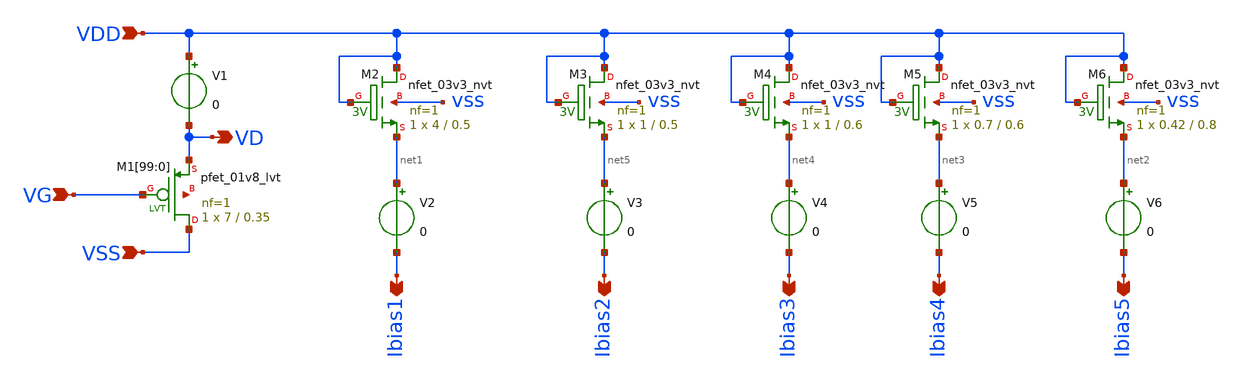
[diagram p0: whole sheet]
** sch_path: design/THESIS_EXP_RO_INVERTER_SKY130A/TB_FET.sch
**.subckt TB_FET VDD VSS VD VG Ibias1 Ibias2 Ibias3 Ibias4 Ibias5
*.ipin VDD
*.ipin VSS
*.opin VD
*.ipin VG
*.opin Ibias1
*.opin Ibias2
*.opin Ibias3
*.opin Ibias4
*.opin Ibias5
V1 VDD VD 0
.save i(v1)
XM1[99] VSS VG VD net6[99] sky130_fd_pr__pfet_01v8_lvt L=0.35 W=7 nf=1 ad='int((1 + 1)/2) * 7 / 1 * 0.29'
+ as='int((1 + 2)/2) * 7 / 1 * 0.29' pd='2*int((1 + 1)/2) * (7 / 1 + 0.29)' ps='2*int((1 + 2)/2) * (7 / 1 + 0.29)'
+ nrd='0.29 / 7 ' nrs='0.29 / 7 ' sa=0 sb=0 sd=0 mult=1 m=1
XM1[98] VSS VG VD net6[98] sky130_fd_pr__pfet_01v8_lvt L=0.35 W=7 nf=1 ad='int((1 + 1)/2) * 7 / 1 * 0.29'
+ as='int((1 + 2)/2) * 7 / 1 * 0.29' pd='2*int((1 + 1)/2) * (7 / 1 + 0.29)' ps='2*int((1 + 2)/2) * (7 / 1 + 0.29)'
+ nrd='0.29 / 7 ' nrs='0.29 / 7 ' sa=0 sb=0 sd=0 mult=1 m=1
XM1[97] VSS VG VD net6[97] sky130_fd_pr__pfet_01v8_lvt L=0.35 W=7 nf=1 ad='int((1 + 1)/2) * 7 / 1 * 0.29'
+ as='int((1 + 2)/2) * 7 / 1 * 0.29' pd='2*int((1 + 1)/2) * (7 / 1 + 0.29)' ps='2*int((1 + 2)/2) * (7 / 1 + 0.29)'
+ nrd='0.29 / 7 ' nrs='0.29 / 7 ' sa=0 sb=0 sd=0 mult=1 m=1
XM1[96] VSS VG VD net6[96] sky130_fd_pr__pfet_01v8_lvt L=0.35 W=7 nf=1 ad='int((1 + 1)/2) * 7 / 1 * 0.29'
+ as='int((1 + 2)/2) * 7 / 1 * 0.29' pd='2*int((1 + 1)/2) * (7 / 1 + 0.29)' ps='2*int((1 + 2)/2) * (7 / 1 + 0.29)'
+ nrd='0.29 / 7 ' nrs='0.29 / 7 ' sa=0 sb=0 sd=0 mult=1 m=1
XM1[95] VSS VG VD net6[95] sky130_fd_pr__pfet_01v8_lvt L=0.35 W=7 nf=1 ad='int((1 + 1)/2) * 7 / 1 * 0.29'
+ as='int((1 + 2)/2) * 7 / 1 * 0.29' pd='2*int((1 + 1)/2) * (7 / 1 + 0.29)' ps='2*int((1 + 2)/2) * (7 / 1 + 0.29)'
+ nrd='0.29 / 7 ' nrs='0.29 / 7 ' sa=0 sb=0 sd=0 mult=1 m=1
XM1[94] VSS VG VD net6[94] sky130_fd_pr__pfet_01v8_lvt L=0.35 W=7 nf=1 ad='int((1 + 1)/2) * 7 / 1 * 0.29'
+ as='int((1 + 2)/2) * 7 / 1 * 0.29' pd='2*int((1 + 1)/2) * (7 / 1 + 0.29)' ps='2*int((1 + 2)/2) * (7 / 1 + 0.29)'
+ nrd='0.29 / 7 ' nrs='0.29 / 7 ' sa=0 sb=0 sd=0 mult=1 m=1
XM1[93] VSS VG VD net6[93] sky130_fd_pr__pfet_01v8_lvt L=0.35 W=7 nf=1 ad='int((1 + 1)/2) * 7 / 1 * 0.29'
+ as='int((1 + 2)/2) * 7 / 1 * 0.29' pd='2*int((1 + 1)/2) * (7 / 1 + 0.29)' ps='2*int((1 + 2)/2) * (7 / 1 + 0.29)'
+ nrd='0.29 / 7 ' nrs='0.29 / 7 ' sa=0 sb=0 sd=0 mult=1 m=1
XM1[92] VSS VG VD net6[92] sky130_fd_pr__pfet_01v8_lvt L=0.35 W=7 nf=1 ad='int((1 + 1)/2) * 7 / 1 * 0.29'
+ as='int((1 + 2)/2) * 7 / 1 * 0.29' pd='2*int((1 + 1)/2) * (7 / 1 + 0.29)' ps='2*int((1 + 2)/2) * (7 / 1 + 0.29)'
+ nrd='0.29 / 7 ' nrs='0.29 / 7 ' sa=0 sb=0 sd=0 mult=1 m=1
XM1[91] VSS VG VD net6[91] sky130_fd_pr__pfet_01v8_lvt L=0.35 W=7 nf=1 ad='int((1 + 1)/2) * 7 / 1 * 0.29'
+ as='int((1 + 2)/2) * 7 / 1 * 0.29' pd='2*int((1 + 1)/2) * (7 / 1 + 0.29)' ps='2*int((1 + 2)/2) * (7 / 1 + 0.29)'
+ nrd='0.29 / 7 ' nrs='0.29 / 7 ' sa=0 sb=0 sd=0 mult=1 m=1
XM1[90] VSS VG VD net6[90] sky130_fd_pr__pfet_01v8_lvt L=0.35 W=7 nf=1 ad='int((1 + 1)/2) * 7 / 1 * 0.29'
+ as='int((1 + 2)/2) * 7 / 1 * 0.29' pd='2*int((1 + 1)/2) * (7 / 1 + 0.29)' ps='2*int((1 + 2)/2) * (7 / 1 + 0.29)'
+ nrd='0.29 / 7 ' nrs='0.29 / 7 ' sa=0 sb=0 sd=0 mult=1 m=1
XM1[89] VSS VG VD net6[89] sky130_fd_pr__pfet_01v8_lvt L=0.35 W=7 nf=1 ad='int((1 + 1)/2) * 7 / 1 * 0.29'
+ as='int((1 + 2)/2) * 7 / 1 * 0.29' pd='2*int((1 + 1)/2) * (7 / 1 + 0.29)' ps='2*int((1 + 2)/2) * (7 / 1 + 0.29)'
+ nrd='0.29 / 7 ' nrs='0.29 / 7 ' sa=0 sb=0 sd=0 mult=1 m=1
XM1[88] VSS VG VD net6[88] sky130_fd_pr__pfet_01v8_lvt L=0.35 W=7 nf=1 ad='int((1 + 1)/2) * 7 / 1 * 0.29'
+ as='int((1 + 2)/2) * 7 / 1 * 0.29' pd='2*int((1 + 1)/2) * (7 / 1 + 0.29)' ps='2*int((1 + 2)/2) * (7 / 1 + 0.29)'
+ nrd='0.29 / 7 ' nrs='0.29 / 7 ' sa=0 sb=0 sd=0 mult=1 m=1
XM1[87] VSS VG VD net6[87] sky130_fd_pr__pfet_01v8_lvt L=0.35 W=7 nf=1 ad='int((1 + 1)/2) * 7 / 1 * 0.29'
+ as='int((1 + 2)/2) * 7 / 1 * 0.29' pd='2*int((1 + 1)/2) * (7 / 1 + 0.29)' ps='2*int((1 + 2)/2) * (7 / 1 + 0.29)'
+ nrd='0.29 / 7 ' nrs='0.29 / 7 ' sa=0 sb=0 sd=0 mult=1 m=1
XM1[86] VSS VG VD net6[86] sky130_fd_pr__pfet_01v8_lvt L=0.35 W=7 nf=1 ad='int((1 + 1)/2) * 7 / 1 * 0.29'
+ as='int((1 + 2)/2) * 7 / 1 * 0.29' pd='2*int((1 + 1)/2) * (7 / 1 + 0.29)' ps='2*int((1 + 2)/2) * (7 / 1 + 0.29)'
+ nrd='0.29 / 7 ' nrs='0.29 / 7 ' sa=0 sb=0 sd=0 mult=1 m=1
XM1[85] VSS VG VD net6[85] sky130_fd_pr__pfet_01v8_lvt L=0.35 W=7 nf=1 ad='int((1 + 1)/2) * 7 / 1 * 0.29'
+ as='int((1 + 2)/2) * 7 / 1 * 0.29' pd='2*int((1 + 1)/2) * (7 / 1 + 0.29)' ps='2*int((1 + 2)/2) * (7 / 1 + 0.29)'
+ nrd='0.29 / 7 ' nrs='0.29 / 7 ' sa=0 sb=0 sd=0 mult=1 m=1
XM1[84] VSS VG VD net6[84] sky130_fd_pr__pfet_01v8_lvt L=0.35 W=7 nf=1 ad='int((1 + 1)/2) * 7 / 1 * 0.29'
+ as='int((1 + 2)/2) * 7 / 1 * 0.29' pd='2*int((1 + 1)/2) * (7 / 1 + 0.29)' ps='2*int((1 + 2)/2) * (7 / 1 + 0.29)'
+ nrd='0.29 / 7 ' nrs='0.29 / 7 ' sa=0 sb=0 sd=0 mult=1 m=1
XM1[83] VSS VG VD net6[83] sky130_fd_pr__pfet_01v8_lvt L=0.35 W=7 nf=1 ad='int((1 + 1)/2) * 7 / 1 * 0.29'
+ as='int((1 + 2)/2) * 7 / 1 * 0.29' pd='2*int((1 + 1)/2) * (7 / 1 + 0.29)' ps='2*int((1 + 2)/2) * (7 / 1 + 0.29)'
+ nrd='0.29 / 7 ' nrs='0.29 / 7 ' sa=0 sb=0 sd=0 mult=1 m=1
XM1[82] VSS VG VD net6[82] sky130_fd_pr__pfet_01v8_lvt L=0.35 W=7 nf=1 ad='int((1 + 1)/2) * 7 / 1 * 0.29'
+ as='int((1 + 2)/2) * 7 / 1 * 0.29' pd='2*int((1 + 1)/2) * (7 / 1 + 0.29)' ps='2*int((1 + 2)/2) * (7 / 1 + 0.29)'
+ nrd='0.29 / 7 ' nrs='0.29 / 7 ' sa=0 sb=0 sd=0 mult=1 m=1
XM1[81] VSS VG VD net6[81] sky130_fd_pr__pfet_01v8_lvt L=0.35 W=7 nf=1 ad='int((1 + 1)/2) * 7 / 1 * 0.29'
+ as='int((1 + 2)/2) * 7 / 1 * 0.29' pd='2*int((1 + 1)/2) * (7 / 1 + 0.29)' ps='2*int((1 + 2)/2) * (7 / 1 + 0.29)'
+ nrd='0.29 / 7 ' nrs='0.29 / 7 ' sa=0 sb=0 sd=0 mult=1 m=1
XM1[80] VSS VG VD net6[80] sky130_fd_pr__pfet_01v8_lvt L=0.35 W=7 nf=1 ad='int((1 + 1)/2) * 7 / 1 * 0.29'
+ as='int((1 + 2)/2) * 7 / 1 * 0.29' pd='2*int((1 + 1)/2) * (7 / 1 + 0.29)' ps='2*int((1 + 2)/2) * (7 / 1 + 0.29)'
+ nrd='0.29 / 7 ' nrs='0.29 / 7 ' sa=0 sb=0 sd=0 mult=1 m=1
XM1[79] VSS VG VD net6[79] sky130_fd_pr__pfet_01v8_lvt L=0.35 W=7 nf=1 ad='int((1 + 1)/2) * 7 / 1 * 0.29'
+ as='int((1 + 2)/2) * 7 / 1 * 0.29' pd='2*int((1 + 1)/2) * (7 / 1 + 0.29)' ps='2*int((1 + 2)/2) * (7 / 1 + 0.29)'
+ nrd='0.29 / 7 ' nrs='0.29 / 7 ' sa=0 sb=0 sd=0 mult=1 m=1
XM1[78] VSS VG VD net6[78] sky130_fd_pr__pfet_01v8_lvt L=0.35 W=7 nf=1 ad='int((1 + 1)/2) * 7 / 1 * 0.29'
+ as='int((1 + 2)/2) * 7 / 1 * 0.29' pd='2*int((1 + 1)/2) * (7 / 1 + 0.29)' ps='2*int((1 + 2)/2) * (7 / 1 + 0.29)'
+ nrd='0.29 / 7 ' nrs='0.29 / 7 ' sa=0 sb=0 sd=0 mult=1 m=1
XM1[77] VSS VG VD net6[77] sky130_fd_pr__pfet_01v8_lvt L=0.35 W=7 nf=1 ad='int((1 + 1)/2) * 7 / 1 * 0.29'
+ as='int((1 + 2)/2) * 7 / 1 * 0.29' pd='2*int((1 + 1)/2) * (7 / 1 + 0.29)' ps='2*int((1 + 2)/2) * (7 / 1 + 0.29)'
+ nrd='0.29 / 7 ' nrs='0.29 / 7 ' sa=0 sb=0 sd=0 mult=1 m=1
XM1[76] VSS VG VD net6[76] sky130_fd_pr__pfet_01v8_lvt L=0.35 W=7 nf=1 ad='int((1 + 1)/2) * 7 / 1 * 0.29'
+ as='int((1 + 2)/2) * 7 / 1 * 0.29' pd='2*int((1 + 1)/2) * (7 / 1 + 0.29)' ps='2*int((1 + 2)/2) * (7 / 1 + 0.29)'
+ nrd='0.29 / 7 ' nrs='0.29 / 7 ' sa=0 sb=0 sd=0 mult=1 m=1
XM1[75] VSS VG VD net6[75] sky130_fd_pr__pfet_01v8_lvt L=0.35 W=7 nf=1 ad='int((1 + 1)/2) * 7 / 1 * 0.29'
+ as='int((1 + 2)/2) * 7 / 1 * 0.29' pd='2*int((1 + 1)/2) * (7 / 1 + 0.29)' ps='2*int((1 + 2)/2) * (7 / 1 + 0.29)'
+ nrd='0.29 / 7 ' nrs='0.29 / 7 ' sa=0 sb=0 sd=0 mult=1 m=1
XM1[74] VSS VG VD net6[74] sky130_fd_pr__pfet_01v8_lvt L=0.35 W=7 nf=1 ad='int((1 + 1)/2) * 7 / 1 * 0.29'
+ as='int((1 + 2)/2) * 7 / 1 * 0.29' pd='2*int((1 + 1)/2) * (7 / 1 + 0.29)' ps='2*int((1 + 2)/2) * (7 / 1 + 0.29)'
+ nrd='0.29 / 7 ' nrs='0.29 / 7 ' sa=0 sb=0 sd=0 mult=1 m=1
XM1[73] VSS VG VD net6[73] sky130_fd_pr__pfet_01v8_lvt L=0.35 W=7 nf=1 ad='int((1 + 1)/2) * 7 / 1 * 0.29'
+ as='int((1 + 2)/2) * 7 / 1 * 0.29' pd='2*int((1 + 1)/2) * (7 / 1 + 0.29)' ps='2*int((1 + 2)/2) * (7 / 1 + 0.29)'
+ nrd='0.29 / 7 ' nrs='0.29 / 7 ' sa=0 sb=0 sd=0 mult=1 m=1
XM1[72] VSS VG VD net6[72] sky130_fd_pr__pfet_01v8_lvt L=0.35 W=7 nf=1 ad='int((1 + 1)/2) * 7 / 1 * 0.29'
+ as='int((1 + 2)/2) * 7 / 1 * 0.29' pd='2*int((1 + 1)/2) * (7 / 1 + 0.29)' ps='2*int((1 + 2)/2) * (7 / 1 + 0.29)'
+ nrd='0.29 / 7 ' nrs='0.29 / 7 ' sa=0 sb=0 sd=0 mult=1 m=1
XM1[71] VSS VG VD net6[71] sky130_fd_pr__pfet_01v8_lvt L=0.35 W=7 nf=1 ad='int((1 + 1)/2) * 7 / 1 * 0.29'
+ as='int((1 + 2)/2) * 7 / 1 * 0.29' pd='2*int((1 + 1)/2) * (7 / 1 + 0.29)' ps='2*int((1 + 2)/2) * (7 / 1 + 0.29)'
+ nrd='0.29 / 7 ' nrs='0.29 / 7 ' sa=0 sb=0 sd=0 mult=1 m=1
XM1[70] VSS VG VD net6[70] sky130_fd_pr__pfet_01v8_lvt L=0.35 W=7 nf=1 ad='int((1 + 1)/2) * 7 / 1 * 0.29'
+ as='int((1 + 2)/2) * 7 / 1 * 0.29' pd='2*int((1 + 1)/2) * (7 / 1 + 0.29)' ps='2*int((1 + 2)/2) * (7 / 1 + 0.29)'
+ nrd='0.29 / 7 ' nrs='0.29 / 7 ' sa=0 sb=0 sd=0 mult=1 m=1
XM1[69] VSS VG VD net6[69] sky130_fd_pr__pfet_01v8_lvt L=0.35 W=7 nf=1 ad='int((1 + 1)/2) * 7 / 1 * 0.29'
+ as='int((1 + 2)/2) * 7 / 1 * 0.29' pd='2*int((1 + 1)/2) * (7 / 1 + 0.29)' ps='2*int((1 + 2)/2) * (7 / 1 + 0.29)'
+ nrd='0.29 / 7 ' nrs='0.29 / 7 ' sa=0 sb=0 sd=0 mult=1 m=1
XM1[68] VSS VG VD net6[68] sky130_fd_pr__pfet_01v8_lvt L=0.35 W=7 nf=1 ad='int((1 + 1)/2) * 7 / 1 * 0.29'
+ as='int((1 + 2)/2) * 7 / 1 * 0.29' pd='2*int((1 + 1)/2) * (7 / 1 + 0.29)' ps='2*int((1 + 2)/2) * (7 / 1 + 0.29)'
+ nrd='0.29 / 7 ' nrs='0.29 / 7 ' sa=0 sb=0 sd=0 mult=1 m=1
XM1[67] VSS VG VD net6[67] sky130_fd_pr__pfet_01v8_lvt L=0.35 W=7 nf=1 ad='int((1 + 1)/2) * 7 / 1 * 0.29'
+ as='int((1 + 2)/2) * 7 / 1 * 0.29' pd='2*int((1 + 1)/2) * (7 / 1 + 0.29)' ps='2*int((1 + 2)/2) * (7 / 1 + 0.29)'
+ nrd='0.29 / 7 ' nrs='0.29 / 7 ' sa=0 sb=0 sd=0 mult=1 m=1
XM1[66] VSS VG VD net6[66] sky130_fd_pr__pfet_01v8_lvt L=0.35 W=7 nf=1 ad='int((1 + 1)/2) * 7 / 1 * 0.29'
+ as='int((1 + 2)/2) * 7 / 1 * 0.29' pd='2*int((1 + 1)/2) * (7 / 1 + 0.29)' ps='2*int((1 + 2)/2) * (7 / 1 + 0.29)'
+ nrd='0.29 / 7 ' nrs='0.29 / 7 ' sa=0 sb=0 sd=0 mult=1 m=1
XM1[65] VSS VG VD net6[65] sky130_fd_pr__pfet_01v8_lvt L=0.35 W=7 nf=1 ad='int((1 + 1)/2) * 7 / 1 * 0.29'
+ as='int((1 + 2)/2) * 7 / 1 * 0.29' pd='2*int((1 + 1)/2) * (7 / 1 + 0.29)' ps='2*int((1 + 2)/2) * (7 / 1 + 0.29)'
+ nrd='0.29 / 7 ' nrs='0.29 / 7 ' sa=0 sb=0 sd=0 mult=1 m=1
XM1[64] VSS VG VD net6[64] sky130_fd_pr__pfet_01v8_lvt L=0.35 W=7 nf=1 ad='int((1 + 1)/2) * 7 / 1 * 0.29'
+ as='int((1 + 2)/2) * 7 / 1 * 0.29' pd='2*int((1 + 1)/2) * (7 / 1 + 0.29)' ps='2*int((1 + 2)/2) * (7 / 1 + 0.29)'
+ nrd='0.29 / 7 ' nrs='0.29 / 7 ' sa=0 sb=0 sd=0 mult=1 m=1
XM1[63] VSS VG VD net6[63] sky130_fd_pr__pfet_01v8_lvt L=0.35 W=7 nf=1 ad='int((1 + 1)/2) * 7 / 1 * 0.29'
+ as='int((1 + 2)/2) * 7 / 1 * 0.29' pd='2*int((1 + 1)/2) * (7 / 1 + 0.29)' ps='2*int((1 + 2)/2) * (7 / 1 + 0.29)'
+ nrd='0.29 / 7 ' nrs='0.29 / 7 ' sa=0 sb=0 sd=0 mult=1 m=1
XM1[62] VSS VG VD net6[62] sky130_fd_pr__pfet_01v8_lvt L=0.35 W=7 nf=1 ad='int((1 + 1)/2) * 7 / 1 * 0.29'
+ as='int((1 + 2)/2) * 7 / 1 * 0.29' pd='2*int((1 + 1)/2) * (7 / 1 + 0.29)' ps='2*int((1 + 2)/2) * (7 / 1 + 0.29)'
+ nrd='0.29 / 7 ' nrs='0.29 / 7 ' sa=0 sb=0 sd=0 mult=1 m=1
XM1[61] VSS VG VD net6[61] sky130_fd_pr__pfet_01v8_lvt L=0.35 W=7 nf=1 ad='int((1 + 1)/2) * 7 / 1 * 0.29'
+ as='int((1 + 2)/2) * 7 / 1 * 0.29' pd='2*int((1 + 1)/2) * (7 / 1 + 0.29)' ps='2*int((1 + 2)/2) * (7 / 1 + 0.29)'
+ nrd='0.29 / 7 ' nrs='0.29 / 7 ' sa=0 sb=0 sd=0 mult=1 m=1
XM1[60] VSS VG VD net6[60] sky130_fd_pr__pfet_01v8_lvt L=0.35 W=7 nf=1 ad='int((1 + 1)/2) * 7 / 1 * 0.29'
+ as='int((1 + 2)/2) * 7 / 1 * 0.29' pd='2*int((1 + 1)/2) * (7 / 1 + 0.29)' ps='2*int((1 + 2)/2) * (7 / 1 + 0.29)'
+ nrd='0.29 / 7 ' nrs='0.29 / 7 ' sa=0 sb=0 sd=0 mult=1 m=1
XM1[59] VSS VG VD net6[59] sky130_fd_pr__pfet_01v8_lvt L=0.35 W=7 nf=1 ad='int((1 + 1)/2) * 7 / 1 * 0.29'
+ as='int((1 + 2)/2) * 7 / 1 * 0.29' pd='2*int((1 + 1)/2) * (7 / 1 + 0.29)' ps='2*int((1 + 2)/2) * (7 / 1 + 0.29)'
+ nrd='0.29 / 7 ' nrs='0.29 / 7 ' sa=0 sb=0 sd=0 mult=1 m=1
XM1[58] VSS VG VD net6[58] sky130_fd_pr__pfet_01v8_lvt L=0.35 W=7 nf=1 ad='int((1 + 1)/2) * 7 / 1 * 0.29'
+ as='int((1 + 2)/2) * 7 / 1 * 0.29' pd='2*int((1 + 1)/2) * (7 / 1 + 0.29)' ps='2*int((1 + 2)/2) * (7 / 1 + 0.29)'
+ nrd='0.29 / 7 ' nrs='0.29 / 7 ' sa=0 sb=0 sd=0 mult=1 m=1
XM1[57] VSS VG VD net6[57] sky130_fd_pr__pfet_01v8_lvt L=0.35 W=7 nf=1 ad='int((1 + 1)/2) * 7 / 1 * 0.29'
+ as='int((1 + 2)/2) * 7 / 1 * 0.29' pd='2*int((1 + 1)/2) * (7 / 1 + 0.29)' ps='2*int((1 + 2)/2) * (7 / 1 + 0.29)'
+ nrd='0.29 / 7 ' nrs='0.29 / 7 ' sa=0 sb=0 sd=0 mult=1 m=1
XM1[56] VSS VG VD net6[56] sky130_fd_pr__pfet_01v8_lvt L=0.35 W=7 nf=1 ad='int((1 + 1)/2) * 7 / 1 * 0.29'
+ as='int((1 + 2)/2) * 7 / 1 * 0.29' pd='2*int((1 + 1)/2) * (7 / 1 + 0.29)' ps='2*int((1 + 2)/2) * (7 / 1 + 0.29)'
+ nrd='0.29 / 7 ' nrs='0.29 / 7 ' sa=0 sb=0 sd=0 mult=1 m=1
XM1[55] VSS VG VD net6[55] sky130_fd_pr__pfet_01v8_lvt L=0.35 W=7 nf=1 ad='int((1 + 1)/2) * 7 / 1 * 0.29'
+ as='int((1 + 2)/2) * 7 / 1 * 0.29' pd='2*int((1 + 1)/2) * (7 / 1 + 0.29)' ps='2*int((1 + 2)/2) * (7 / 1 + 0.29)'
+ nrd='0.29 / 7 ' nrs='0.29 / 7 ' sa=0 sb=0 sd=0 mult=1 m=1
XM1[54] VSS VG VD net6[54] sky130_fd_pr__pfet_01v8_lvt L=0.35 W=7 nf=1 ad='int((1 + 1)/2) * 7 / 1 * 0.29'
+ as='int((1 + 2)/2) * 7 / 1 * 0.29' pd='2*int((1 + 1)/2) * (7 / 1 + 0.29)' ps='2*int((1 + 2)/2) * (7 / 1 + 0.29)'
+ nrd='0.29 / 7 ' nrs='0.29 / 7 ' sa=0 sb=0 sd=0 mult=1 m=1
XM1[53] VSS VG VD net6[53] sky130_fd_pr__pfet_01v8_lvt L=0.35 W=7 nf=1 ad='int((1 + 1)/2) * 7 / 1 * 0.29'
+ as='int((1 + 2)/2) * 7 / 1 * 0.29' pd='2*int((1 + 1)/2) * (7 / 1 + 0.29)' ps='2*int((1 + 2)/2) * (7 / 1 + 0.29)'
+ nrd='0.29 / 7 ' nrs='0.29 / 7 ' sa=0 sb=0 sd=0 mult=1 m=1
XM1[52] VSS VG VD net6[52] sky130_fd_pr__pfet_01v8_lvt L=0.35 W=7 nf=1 ad='int((1 + 1)/2) * 7 / 1 * 0.29'
+ as='int((1 + 2)/2) * 7 / 1 * 0.29' pd='2*int((1 + 1)/2) * (7 / 1 + 0.29)' ps='2*int((1 + 2)/2) * (7 / 1 + 0.29)'
+ nrd='0.29 / 7 ' nrs='0.29 / 7 ' sa=0 sb=0 sd=0 mult=1 m=1
XM1[51] VSS VG VD net6[51] sky130_fd_pr__pfet_01v8_lvt L=0.35 W=7 nf=1 ad='int((1 + 1)/2) * 7 / 1 * 0.29'
+ as='int((1 + 2)/2) * 7 / 1 * 0.29' pd='2*int((1 + 1)/2) * (7 / 1 + 0.29)' ps='2*int((1 + 2)/2) * (7 / 1 + 0.29)'
+ nrd='0.29 / 7 ' nrs='0.29 / 7 ' sa=0 sb=0 sd=0 mult=1 m=1
XM1[50] VSS VG VD net6[50] sky130_fd_pr__pfet_01v8_lvt L=0.35 W=7 nf=1 ad='int((1 + 1)/2) * 7 / 1 * 0.29'
+ as='int((1 + 2)/2) * 7 / 1 * 0.29' pd='2*int((1 + 1)/2) * (7 / 1 + 0.29)' ps='2*int((1 + 2)/2) * (7 / 1 + 0.29)'
+ nrd='0.29 / 7 ' nrs='0.29 / 7 ' sa=0 sb=0 sd=0 mult=1 m=1
XM1[49] VSS VG VD net6[49] sky130_fd_pr__pfet_01v8_lvt L=0.35 W=7 nf=1 ad='int((1 + 1)/2) * 7 / 1 * 0.29'
+ as='int((1 + 2)/2) * 7 / 1 * 0.29' pd='2*int((1 + 1)/2) * (7 / 1 + 0.29)' ps='2*int((1 + 2)/2) * (7 / 1 + 0.29)'
+ nrd='0.29 / 7 ' nrs='0.29 / 7 ' sa=0 sb=0 sd=0 mult=1 m=1
XM1[48] VSS VG VD net6[48] sky130_fd_pr__pfet_01v8_lvt L=0.35 W=7 nf=1 ad='int((1 + 1)/2) * 7 / 1 * 0.29'
+ as='int((1 + 2)/2) * 7 / 1 * 0.29' pd='2*int((1 + 1)/2) * (7 / 1 + 0.29)' ps='2*int((1 + 2)/2) * (7 / 1 + 0.29)'
+ nrd='0.29 / 7 ' nrs='0.29 / 7 ' sa=0 sb=0 sd=0 mult=1 m=1
XM1[47] VSS VG VD net6[47] sky130_fd_pr__pfet_01v8_lvt L=0.35 W=7 nf=1 ad='int((1 + 1)/2) * 7 / 1 * 0.29'
+ as='int((1 + 2)/2) * 7 / 1 * 0.29' pd='2*int((1 + 1)/2) * (7 / 1 + 0.29)' ps='2*int((1 + 2)/2) * (7 / 1 + 0.29)'
+ nrd='0.29 / 7 ' nrs='0.29 / 7 ' sa=0 sb=0 sd=0 mult=1 m=1
XM1[46] VSS VG VD net6[46] sky130_fd_pr__pfet_01v8_lvt L=0.35 W=7 nf=1 ad='int((1 + 1)/2) * 7 / 1 * 0.29'
+ as='int((1 + 2)/2) * 7 / 1 * 0.29' pd='2*int((1 + 1)/2) * (7 / 1 + 0.29)' ps='2*int((1 + 2)/2) * (7 / 1 + 0.29)'
+ nrd='0.29 / 7 ' nrs='0.29 / 7 ' sa=0 sb=0 sd=0 mult=1 m=1
XM1[45] VSS VG VD net6[45] sky130_fd_pr__pfet_01v8_lvt L=0.35 W=7 nf=1 ad='int((1 + 1)/2) * 7 / 1 * 0.29'
+ as='int((1 + 2)/2) * 7 / 1 * 0.29' pd='2*int((1 + 1)/2) * (7 / 1 + 0.29)' ps='2*int((1 + 2)/2) * (7 / 1 + 0.29)'
+ nrd='0.29 / 7 ' nrs='0.29 / 7 ' sa=0 sb=0 sd=0 mult=1 m=1
XM1[44] VSS VG VD net6[44] sky130_fd_pr__pfet_01v8_lvt L=0.35 W=7 nf=1 ad='int((1 + 1)/2) * 7 / 1 * 0.29'
+ as='int((1 + 2)/2) * 7 / 1 * 0.29' pd='2*int((1 + 1)/2) * (7 / 1 + 0.29)' ps='2*int((1 + 2)/2) * (7 / 1 + 0.29)'
+ nrd='0.29 / 7 ' nrs='0.29 / 7 ' sa=0 sb=0 sd=0 mult=1 m=1
XM1[43] VSS VG VD net6[43] sky130_fd_pr__pfet_01v8_lvt L=0.35 W=7 nf=1 ad='int((1 + 1)/2) * 7 / 1 * 0.29'
+ as='int((1 + 2)/2) * 7 / 1 * 0.29' pd='2*int((1 + 1)/2) * (7 / 1 + 0.29)' ps='2*int((1 + 2)/2) * (7 / 1 + 0.29)'
+ nrd='0.29 / 7 ' nrs='0.29 / 7 ' sa=0 sb=0 sd=0 mult=1 m=1
XM1[42] VSS VG VD net6[42] sky130_fd_pr__pfet_01v8_lvt L=0.35 W=7 nf=1 ad='int((1 + 1)/2) * 7 / 1 * 0.29'
+ as='int((1 + 2)/2) * 7 / 1 * 0.29' pd='2*int((1 + 1)/2) * (7 / 1 + 0.29)' ps='2*int((1 + 2)/2) * (7 / 1 + 0.29)'
+ nrd='0.29 / 7 ' nrs='0.29 / 7 ' sa=0 sb=0 sd=0 mult=1 m=1
XM1[41] VSS VG VD net6[41] sky130_fd_pr__pfet_01v8_lvt L=0.35 W=7 nf=1 ad='int((1 + 1)/2) * 7 / 1 * 0.29'
+ as='int((1 + 2)/2) * 7 / 1 * 0.29' pd='2*int((1 + 1)/2) * (7 / 1 + 0.29)' ps='2*int((1 + 2)/2) * (7 / 1 + 0.29)'
+ nrd='0.29 / 7 ' nrs='0.29 / 7 ' sa=0 sb=0 sd=0 mult=1 m=1
XM1[40] VSS VG VD net6[40] sky130_fd_pr__pfet_01v8_lvt L=0.35 W=7 nf=1 ad='int((1 + 1)/2) * 7 / 1 * 0.29'
+ as='int((1 + 2)/2) * 7 / 1 * 0.29' pd='2*int((1 + 1)/2) * (7 / 1 + 0.29)' ps='2*int((1 + 2)/2) * (7 / 1 + 0.29)'
+ nrd='0.29 / 7 ' nrs='0.29 / 7 ' sa=0 sb=0 sd=0 mult=1 m=1
XM1[39] VSS VG VD net6[39] sky130_fd_pr__pfet_01v8_lvt L=0.35 W=7 nf=1 ad='int((1 + 1)/2) * 7 / 1 * 0.29'
+ as='int((1 + 2)/2) * 7 / 1 * 0.29' pd='2*int((1 + 1)/2) * (7 / 1 + 0.29)' ps='2*int((1 + 2)/2) * (7 / 1 + 0.29)'
+ nrd='0.29 / 7 ' nrs='0.29 / 7 ' sa=0 sb=0 sd=0 mult=1 m=1
XM1[38] VSS VG VD net6[38] sky130_fd_pr__pfet_01v8_lvt L=0.35 W=7 nf=1 ad='int((1 + 1)/2) * 7 / 1 * 0.29'
+ as='int((1 + 2)/2) * 7 / 1 * 0.29' pd='2*int((1 + 1)/2) * (7 / 1 + 0.29)' ps='2*int((1 + 2)/2) * (7 / 1 + 0.29)'
+ nrd='0.29 / 7 ' nrs='0.29 / 7 ' sa=0 sb=0 sd=0 mult=1 m=1
XM1[37] VSS VG VD net6[37] sky130_fd_pr__pfet_01v8_lvt L=0.35 W=7 nf=1 ad='int((1 + 1)/2) * 7 / 1 * 0.29'
+ as='int((1 + 2)/2) * 7 / 1 * 0.29' pd='2*int((1 + 1)/2) * (7 / 1 + 0.29)' ps='2*int((1 + 2)/2) * (7 / 1 + 0.29)'
+ nrd='0.29 / 7 ' nrs='0.29 / 7 ' sa=0 sb=0 sd=0 mult=1 m=1
XM1[36] VSS VG VD net6[36] sky130_fd_pr__pfet_01v8_lvt L=0.35 W=7 nf=1 ad='int((1 + 1)/2) * 7 / 1 * 0.29'
+ as='int((1 + 2)/2) * 7 / 1 * 0.29' pd='2*int((1 + 1)/2) * (7 / 1 + 0.29)' ps='2*int((1 + 2)/2) * (7 / 1 + 0.29)'
+ nrd='0.29 / 7 ' nrs='0.29 / 7 ' sa=0 sb=0 sd=0 mult=1 m=1
XM1[35] VSS VG VD net6[35] sky130_fd_pr__pfet_01v8_lvt L=0.35 W=7 nf=1 ad='int((1 + 1)/2) * 7 / 1 * 0.29'
+ as='int((1 + 2)/2) * 7 / 1 * 0.29' pd='2*int((1 + 1)/2) * (7 / 1 + 0.29)' ps='2*int((1 + 2)/2) * (7 / 1 + 0.29)'
+ nrd='0.29 / 7 ' nrs='0.29 / 7 ' sa=0 sb=0 sd=0 mult=1 m=1
XM1[34] VSS VG VD net6[34] sky130_fd_pr__pfet_01v8_lvt L=0.35 W=7 nf=1 ad='int((1 + 1)/2) * 7 / 1 * 0.29'
+ as='int((1 + 2)/2) * 7 / 1 * 0.29' pd='2*int((1 + 1)/2) * (7 / 1 + 0.29)' ps='2*int((1 + 2)/2) * (7 / 1 + 0.29)'
+ nrd='0.29 / 7 ' nrs='0.29 / 7 ' sa=0 sb=0 sd=0 mult=1 m=1
XM1[33] VSS VG VD net6[33] sky130_fd_pr__pfet_01v8_lvt L=0.35 W=7 nf=1 ad='int((1 + 1)/2) * 7 / 1 * 0.29'
+ as='int((1 + 2)/2) * 7 / 1 * 0.29' pd='2*int((1 + 1)/2) * (7 / 1 + 0.29)' ps='2*int((1 + 2)/2) * (7 / 1 + 0.29)'
+ nrd='0.29 / 7 ' nrs='0.29 / 7 ' sa=0 sb=0 sd=0 mult=1 m=1
XM1[32] VSS VG VD net6[32] sky130_fd_pr__pfet_01v8_lvt L=0.35 W=7 nf=1 ad='int((1 + 1)/2) * 7 / 1 * 0.29'
+ as='int((1 + 2)/2) * 7 / 1 * 0.29' pd='2*int((1 + 1)/2) * (7 / 1 + 0.29)' ps='2*int((1 + 2)/2) * (7 / 1 + 0.29)'
+ nrd='0.29 / 7 ' nrs='0.29 / 7 ' sa=0 sb=0 sd=0 mult=1 m=1
XM1[31] VSS VG VD net6[31] sky130_fd_pr__pfet_01v8_lvt L=0.35 W=7 nf=1 ad='int((1 + 1)/2) * 7 / 1 * 0.29'
+ as='int((1 + 2)/2) * 7 / 1 * 0.29' pd='2*int((1 + 1)/2) * (7 / 1 + 0.29)' ps='2*int((1 + 2)/2) * (7 / 1 + 0.29)'
+ nrd='0.29 / 7 ' nrs='0.29 / 7 ' sa=0 sb=0 sd=0 mult=1 m=1
XM1[30] VSS VG VD net6[30] sky130_fd_pr__pfet_01v8_lvt L=0.35 W=7 nf=1 ad='int((1 + 1)/2) * 7 / 1 * 0.29'
+ as='int((1 + 2)/2) * 7 / 1 * 0.29' pd='2*int((1 + 1)/2) * (7 / 1 + 0.29)' ps='2*int((1 + 2)/2) * (7 / 1 + 0.29)'
+ nrd='0.29 / 7 ' nrs='0.29 / 7 ' sa=0 sb=0 sd=0 mult=1 m=1
XM1[29] VSS VG VD net6[29] sky130_fd_pr__pfet_01v8_lvt L=0.35 W=7 nf=1 ad='int((1 + 1)/2) * 7 / 1 * 0.29'
+ as='int((1 + 2)/2) * 7 / 1 * 0.29' pd='2*int((1 + 1)/2) * (7 / 1 + 0.29)' ps='2*int((1 + 2)/2) * (7 / 1 + 0.29)'
+ nrd='0.29 / 7 ' nrs='0.29 / 7 ' sa=0 sb=0 sd=0 mult=1 m=1
XM1[28] VSS VG VD net6[28] sky130_fd_pr__pfet_01v8_lvt L=0.35 W=7 nf=1 ad='int((1 + 1)/2) * 7 / 1 * 0.29'
+ as='int((1 + 2)/2) * 7 / 1 * 0.29' pd='2*int((1 + 1)/2) * (7 / 1 + 0.29)' ps='2*int((1 + 2)/2) * (7 / 1 + 0.29)'
+ nrd='0.29 / 7 ' nrs='0.29 / 7 ' sa=0 sb=0 sd=0 mult=1 m=1
XM1[27] VSS VG VD net6[27] sky130_fd_pr__pfet_01v8_lvt L=0.35 W=7 nf=1 ad='int((1 + 1)/2) * 7 / 1 * 0.29'
+ as='int((1 + 2)/2) * 7 / 1 * 0.29' pd='2*int((1 + 1)/2) * (7 / 1 + 0.29)' ps='2*int((1 + 2)/2) * (7 / 1 + 0.29)'
+ nrd='0.29 / 7 ' nrs='0.29 / 7 ' sa=0 sb=0 sd=0 mult=1 m=1
XM1[26] VSS VG VD net6[26] sky130_fd_pr__pfet_01v8_lvt L=0.35 W=7 nf=1 ad='int((1 + 1)/2) * 7 / 1 * 0.29'
+ as='int((1 + 2)/2) * 7 / 1 * 0.29' pd='2*int((1 + 1)/2) * (7 / 1 + 0.29)' ps='2*int((1 + 2)/2) * (7 / 1 + 0.29)'
+ nrd='0.29 / 7 ' nrs='0.29 / 7 ' sa=0 sb=0 sd=0 mult=1 m=1
XM1[25] VSS VG VD net6[25] sky130_fd_pr__pfet_01v8_lvt L=0.35 W=7 nf=1 ad='int((1 + 1)/2) * 7 / 1 * 0.29'
+ as='int((1 + 2)/2) * 7 / 1 * 0.29' pd='2*int((1 + 1)/2) * (7 / 1 + 0.29)' ps='2*int((1 + 2)/2) * (7 / 1 + 0.29)'
+ nrd='0.29 / 7 ' nrs='0.29 / 7 ' sa=0 sb=0 sd=0 mult=1 m=1
XM1[24] VSS VG VD net6[24] sky130_fd_pr__pfet_01v8_lvt L=0.35 W=7 nf=1 ad='int((1 + 1)/2) * 7 / 1 * 0.29'
+ as='int((1 + 2)/2) * 7 / 1 * 0.29' pd='2*int((1 + 1)/2) * (7 / 1 + 0.29)' ps='2*int((1 + 2)/2) * (7 / 1 + 0.29)'
+ nrd='0.29 / 7 ' nrs='0.29 / 7 ' sa=0 sb=0 sd=0 mult=1 m=1
XM1[23] VSS VG VD net6[23] sky130_fd_pr__pfet_01v8_lvt L=0.35 W=7 nf=1 ad='int((1 + 1)/2) * 7 / 1 * 0.29'
+ as='int((1 + 2)/2) * 7 / 1 * 0.29' pd='2*int((1 + 1)/2) * (7 / 1 + 0.29)' ps='2*int((1 + 2)/2) * (7 / 1 + 0.29)'
+ nrd='0.29 / 7 ' nrs='0.29 / 7 ' sa=0 sb=0 sd=0 mult=1 m=1
XM1[22] VSS VG VD net6[22] sky130_fd_pr__pfet_01v8_lvt L=0.35 W=7 nf=1 ad='int((1 + 1)/2) * 7 / 1 * 0.29'
+ as='int((1 + 2)/2) * 7 / 1 * 0.29' pd='2*int((1 + 1)/2) * (7 / 1 + 0.29)' ps='2*int((1 + 2)/2) * (7 / 1 + 0.29)'
+ nrd='0.29 / 7 ' nrs='0.29 / 7 ' sa=0 sb=0 sd=0 mult=1 m=1
XM1[21] VSS VG VD net6[21] sky130_fd_pr__pfet_01v8_lvt L=0.35 W=7 nf=1 ad='int((1 + 1)/2) * 7 / 1 * 0.29'
+ as='int((1 + 2)/2) * 7 / 1 * 0.29' pd='2*int((1 + 1)/2) * (7 / 1 + 0.29)' ps='2*int((1 + 2)/2) * (7 / 1 + 0.29)'
+ nrd='0.29 / 7 ' nrs='0.29 / 7 ' sa=0 sb=0 sd=0 mult=1 m=1
XM1[20] VSS VG VD net6[20] sky130_fd_pr__pfet_01v8_lvt L=0.35 W=7 nf=1 ad='int((1 + 1)/2) * 7 / 1 * 0.29'
+ as='int((1 + 2)/2) * 7 / 1 * 0.29' pd='2*int((1 + 1)/2) * (7 / 1 + 0.29)' ps='2*int((1 + 2)/2) * (7 / 1 + 0.29)'
+ nrd='0.29 / 7 ' nrs='0.29 / 7 ' sa=0 sb=0 sd=0 mult=1 m=1
XM1[19] VSS VG VD net6[19] sky130_fd_pr__pfet_01v8_lvt L=0.35 W=7 nf=1 ad='int((1 + 1)/2) * 7 / 1 * 0.29'
+ as='int((1 + 2)/2) * 7 / 1 * 0.29' pd='2*int((1 + 1)/2) * (7 / 1 + 0.29)' ps='2*int((1 + 2)/2) * (7 / 1 + 0.29)'
+ nrd='0.29 / 7 ' nrs='0.29 / 7 ' sa=0 sb=0 sd=0 mult=1 m=1
XM1[18] VSS VG VD net6[18] sky130_fd_pr__pfet_01v8_lvt L=0.35 W=7 nf=1 ad='int((1 + 1)/2) * 7 / 1 * 0.29'
+ as='int((1 + 2)/2) * 7 / 1 * 0.29' pd='2*int((1 + 1)/2) * (7 / 1 + 0.29)' ps='2*int((1 + 2)/2) * (7 / 1 + 0.29)'
+ nrd='0.29 / 7 ' nrs='0.29 / 7 ' sa=0 sb=0 sd=0 mult=1 m=1
XM1[17] VSS VG VD net6[17] sky130_fd_pr__pfet_01v8_lvt L=0.35 W=7 nf=1 ad='int((1 + 1)/2) * 7 / 1 * 0.29'
+ as='int((1 + 2)/2) * 7 / 1 * 0.29' pd='2*int((1 + 1)/2) * (7 / 1 + 0.29)' ps='2*int((1 + 2)/2) * (7 / 1 + 0.29)'
+ nrd='0.29 / 7 ' nrs='0.29 / 7 ' sa=0 sb=0 sd=0 mult=1 m=1
XM1[16] VSS VG VD net6[16] sky130_fd_pr__pfet_01v8_lvt L=0.35 W=7 nf=1 ad='int((1 + 1)/2) * 7 / 1 * 0.29'
+ as='int((1 + 2)/2) * 7 / 1 * 0.29' pd='2*int((1 + 1)/2) * (7 / 1 + 0.29)' ps='2*int((1 + 2)/2) * (7 / 1 + 0.29)'
+ nrd='0.29 / 7 ' nrs='0.29 / 7 ' sa=0 sb=0 sd=0 mult=1 m=1
XM1[15] VSS VG VD net6[15] sky130_fd_pr__pfet_01v8_lvt L=0.35 W=7 nf=1 ad='int((1 + 1)/2) * 7 / 1 * 0.29'
+ as='int((1 + 2)/2) * 7 / 1 * 0.29' pd='2*int((1 + 1)/2) * (7 / 1 + 0.29)' ps='2*int((1 + 2)/2) * (7 / 1 + 0.29)'
+ nrd='0.29 / 7 ' nrs='0.29 / 7 ' sa=0 sb=0 sd=0 mult=1 m=1
XM1[14] VSS VG VD net6[14] sky130_fd_pr__pfet_01v8_lvt L=0.35 W=7 nf=1 ad='int((1 + 1)/2) * 7 / 1 * 0.29'
+ as='int((1 + 2)/2) * 7 / 1 * 0.29' pd='2*int((1 + 1)/2) * (7 / 1 + 0.29)' ps='2*int((1 + 2)/2) * (7 / 1 + 0.29)'
+ nrd='0.29 / 7 ' nrs='0.29 / 7 ' sa=0 sb=0 sd=0 mult=1 m=1
XM1[13] VSS VG VD net6[13] sky130_fd_pr__pfet_01v8_lvt L=0.35 W=7 nf=1 ad='int((1 + 1)/2) * 7 / 1 * 0.29'
+ as='int((1 + 2)/2) * 7 / 1 * 0.29' pd='2*int((1 + 1)/2) * (7 / 1 + 0.29)' ps='2*int((1 + 2)/2) * (7 / 1 + 0.29)'
+ nrd='0.29 / 7 ' nrs='0.29 / 7 ' sa=0 sb=0 sd=0 mult=1 m=1
XM1[12] VSS VG VD net6[12] sky130_fd_pr__pfet_01v8_lvt L=0.35 W=7 nf=1 ad='int((1 + 1)/2) * 7 / 1 * 0.29'
+ as='int((1 + 2)/2) * 7 / 1 * 0.29' pd='2*int((1 + 1)/2) * (7 / 1 + 0.29)' ps='2*int((1 + 2)/2) * (7 / 1 + 0.29)'
+ nrd='0.29 / 7 ' nrs='0.29 / 7 ' sa=0 sb=0 sd=0 mult=1 m=1
XM1[11] VSS VG VD net6[11] sky130_fd_pr__pfet_01v8_lvt L=0.35 W=7 nf=1 ad='int((1 + 1)/2) * 7 / 1 * 0.29'
+ as='int((1 + 2)/2) * 7 / 1 * 0.29' pd='2*int((1 + 1)/2) * (7 / 1 + 0.29)' ps='2*int((1 + 2)/2) * (7 / 1 + 0.29)'
+ nrd='0.29 / 7 ' nrs='0.29 / 7 ' sa=0 sb=0 sd=0 mult=1 m=1
XM1[10] VSS VG VD net6[10] sky130_fd_pr__pfet_01v8_lvt L=0.35 W=7 nf=1 ad='int((1 + 1)/2) * 7 / 1 * 0.29'
+ as='int((1 + 2)/2) * 7 / 1 * 0.29' pd='2*int((1 + 1)/2) * (7 / 1 + 0.29)' ps='2*int((1 + 2)/2) * (7 / 1 + 0.29)'
+ nrd='0.29 / 7 ' nrs='0.29 / 7 ' sa=0 sb=0 sd=0 mult=1 m=1
XM1[9] VSS VG VD net6[9] sky130_fd_pr__pfet_01v8_lvt L=0.35 W=7 nf=1 ad='int((1 + 1)/2) * 7 / 1 * 0.29'
+ as='int((1 + 2)/2) * 7 / 1 * 0.29' pd='2*int((1 + 1)/2) * (7 / 1 + 0.29)' ps='2*int((1 + 2)/2) * (7 / 1 + 0.29)'
+ nrd='0.29 / 7 ' nrs='0.29 / 7 ' sa=0 sb=0 sd=0 mult=1 m=1
XM1[8] VSS VG VD net6[8] sky130_fd_pr__pfet_01v8_lvt L=0.35 W=7 nf=1 ad='int((1 + 1)/2) * 7 / 1 * 0.29'
+ as='int((1 + 2)/2) * 7 / 1 * 0.29' pd='2*int((1 + 1)/2) * (7 / 1 + 0.29)' ps='2*int((1 + 2)/2) * (7 / 1 + 0.29)'
+ nrd='0.29 / 7 ' nrs='0.29 / 7 ' sa=0 sb=0 sd=0 mult=1 m=1
XM1[7] VSS VG VD net6[7] sky130_fd_pr__pfet_01v8_lvt L=0.35 W=7 nf=1 ad='int((1 + 1)/2) * 7 / 1 * 0.29'
+ as='int((1 + 2)/2) * 7 / 1 * 0.29' pd='2*int((1 + 1)/2) * (7 / 1 + 0.29)' ps='2*int((1 + 2)/2) * (7 / 1 + 0.29)'
+ nrd='0.29 / 7 ' nrs='0.29 / 7 ' sa=0 sb=0 sd=0 mult=1 m=1
XM1[6] VSS VG VD net6[6] sky130_fd_pr__pfet_01v8_lvt L=0.35 W=7 nf=1 ad='int((1 + 1)/2) * 7 / 1 * 0.29'
+ as='int((1 + 2)/2) * 7 / 1 * 0.29' pd='2*int((1 + 1)/2) * (7 / 1 + 0.29)' ps='2*int((1 + 2)/2) * (7 / 1 + 0.29)'
+ nrd='0.29 / 7 ' nrs='0.29 / 7 ' sa=0 sb=0 sd=0 mult=1 m=1
XM1[5] VSS VG VD net6[5] sky130_fd_pr__pfet_01v8_lvt L=0.35 W=7 nf=1 ad='int((1 + 1)/2) * 7 / 1 * 0.29'
+ as='int((1 + 2)/2) * 7 / 1 * 0.29' pd='2*int((1 + 1)/2) * (7 / 1 + 0.29)' ps='2*int((1 + 2)/2) * (7 / 1 + 0.29)'
+ nrd='0.29 / 7 ' nrs='0.29 / 7 ' sa=0 sb=0 sd=0 mult=1 m=1
XM1[4] VSS VG VD net6[4] sky130_fd_pr__pfet_01v8_lvt L=0.35 W=7 nf=1 ad='int((1 + 1)/2) * 7 / 1 * 0.29'
+ as='int((1 + 2)/2) * 7 / 1 * 0.29' pd='2*int((1 + 1)/2) * (7 / 1 + 0.29)' ps='2*int((1 + 2)/2) * (7 / 1 + 0.29)'
+ nrd='0.29 / 7 ' nrs='0.29 / 7 ' sa=0 sb=0 sd=0 mult=1 m=1
XM1[3] VSS VG VD net6[3] sky130_fd_pr__pfet_01v8_lvt L=0.35 W=7 nf=1 ad='int((1 + 1)/2) * 7 / 1 * 0.29'
+ as='int((1 + 2)/2) * 7 / 1 * 0.29' pd='2*int((1 + 1)/2) * (7 / 1 + 0.29)' ps='2*int((1 + 2)/2) * (7 / 1 + 0.29)'
+ nrd='0.29 / 7 ' nrs='0.29 / 7 ' sa=0 sb=0 sd=0 mult=1 m=1
XM1[2] VSS VG VD net6[2] sky130_fd_pr__pfet_01v8_lvt L=0.35 W=7 nf=1 ad='int((1 + 1)/2) * 7 / 1 * 0.29'
+ as='int((1 + 2)/2) * 7 / 1 * 0.29' pd='2*int((1 + 1)/2) * (7 / 1 + 0.29)' ps='2*int((1 + 2)/2) * (7 / 1 + 0.29)'
+ nrd='0.29 / 7 ' nrs='0.29 / 7 ' sa=0 sb=0 sd=0 mult=1 m=1
XM1[1] VSS VG VD net6[1] sky130_fd_pr__pfet_01v8_lvt L=0.35 W=7 nf=1 ad='int((1 + 1)/2) * 7 / 1 * 0.29'
+ as='int((1 + 2)/2) * 7 / 1 * 0.29' pd='2*int((1 + 1)/2) * (7 / 1 + 0.29)' ps='2*int((1 + 2)/2) * (7 / 1 + 0.29)'
+ nrd='0.29 / 7 ' nrs='0.29 / 7 ' sa=0 sb=0 sd=0 mult=1 m=1
XM1[0] VSS VG VD net6[0] sky130_fd_pr__pfet_01v8_lvt L=0.35 W=7 nf=1 ad='int((1 + 1)/2) * 7 / 1 * 0.29'
+ as='int((1 + 2)/2) * 7 / 1 * 0.29' pd='2*int((1 + 1)/2) * (7 / 1 + 0.29)' ps='2*int((1 + 2)/2) * (7 / 1 + 0.29)'
+ nrd='0.29 / 7 ' nrs='0.29 / 7 ' sa=0 sb=0 sd=0 mult=1 m=1
XM2 VDD VDD net1 vss sky130_fd_pr__nfet_03v3_nvt L=0.5 W=4 nf=1 ad='int((nf+1)/2) * W/nf * 0.29' as='int((nf+2)/2) * W/nf * 0.29'
+ pd='2*int((nf+1)/2) * (W/nf + 0.29)' ps='2*int((nf+2)/2) * (W/nf + 0.29)' nrd='0.29 / W' nrs='0.29 / W'
+ sa=0 sb=0 sd=0 mult=1 m=1
V2 net1 Ibias1 0
.save i(v2)
XM3 VDD VDD net5 vss sky130_fd_pr__nfet_03v3_nvt L=0.5 W=1 nf=1 ad='int((nf+1)/2) * W/nf * 0.29' as='int((nf+2)/2) * W/nf * 0.29'
+ pd='2*int((nf+1)/2) * (W/nf + 0.29)' ps='2*int((nf+2)/2) * (W/nf + 0.29)' nrd='0.29 / W' nrs='0.29 / W'
+ sa=0 sb=0 sd=0 mult=1 m=1
XM4 VDD VDD net4 vss sky130_fd_pr__nfet_03v3_nvt L=0.6 W=1 nf=1 ad='int((nf+1)/2) * W/nf * 0.29' as='int((nf+2)/2) * W/nf * 0.29'
+ pd='2*int((nf+1)/2) * (W/nf + 0.29)' ps='2*int((nf+2)/2) * (W/nf + 0.29)' nrd='0.29 / W' nrs='0.29 / W'
+ sa=0 sb=0 sd=0 mult=1 m=1
XM5 VDD VDD net3 vss sky130_fd_pr__nfet_03v3_nvt L=0.6 W=0.7 nf=1 ad='int((nf+1)/2) * W/nf * 0.29' as='int((nf+2)/2) * W/nf * 0.29'
+ pd='2*int((nf+1)/2) * (W/nf + 0.29)' ps='2*int((nf+2)/2) * (W/nf + 0.29)' nrd='0.29 / W' nrs='0.29 / W'
+ sa=0 sb=0 sd=0 mult=1 m=1
V3 net5 Ibias2 0
.save i(v3)
V4 net4 Ibias3 0
.save i(v4)
V5 net3 Ibias4 0
.save i(v5)
XM6 VDD VDD net2 vss sky130_fd_pr__nfet_03v3_nvt L=0.8 W=0.42 nf=1 ad='int((nf+1)/2) * W/nf * 0.29' as='int((nf+2)/2) * W/nf * 0.29'
+ pd='2*int((nf+1)/2) * (W/nf + 0.29)' ps='2*int((nf+2)/2) * (W/nf + 0.29)' nrd='0.29 / W' nrs='0.29 / W'
+ sa=0 sb=0 sd=0 mult=1 m=1
V6 net2 Ibias5 0
.save i(v6)
**.ends
.end
